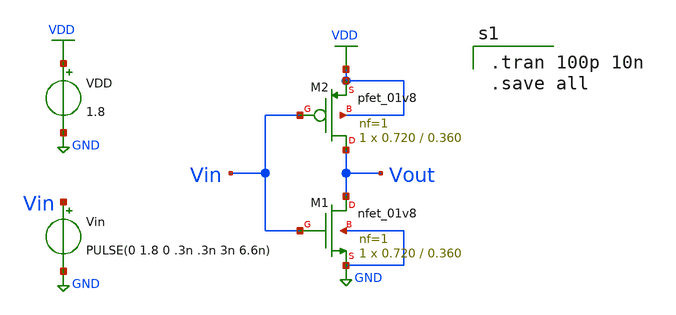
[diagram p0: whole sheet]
** sch_path: xschem/inverter/inverter_squarewave.sch
**.subckt inverter_squarewave
VDD VDD GND 1.8
Vin Vin GND PULSE(0 1.8 0 .3n .3n 3n 6.6n)
XM1 Vout Vin GND GND sky130_fd_pr__nfet_01v8 L=0.360 W=0.720 nf=1 ad='int((nf+1)/2) * W/nf * 0.29' as='int((nf+2)/2) * W/nf * 0.29'
+ pd='2*int((nf+1)/2) * (W/nf + 0.29)' ps='2*int((nf+2)/2) * (W/nf + 0.29)' nrd='0.29 / W' nrs='0.29 / W'
+ sa=0 sb=0 sd=0 mult=1 m=1
XM2 Vout Vin VDD VDD sky130_fd_pr__pfet_01v8 L=0.360 W=0.720 nf=1 ad='int((nf+1)/2) * W/nf * 0.29' as='int((nf+2)/2) * W/nf * 0.29'
+ pd='2*int((nf+1)/2) * (W/nf + 0.29)' ps='2*int((nf+2)/2) * (W/nf + 0.29)' nrd='0.29 / W' nrs='0.29 / W'
+ sa=0 sb=0 sd=0 mult=1 m=1
**** begin user architecture code

.tran 100p 10n
.save all


** opencircuitdesign pdks install
.lib $::SKYWATER_MODELS/sky130.lib.spice tt


**** end user architecture code
**.ends
.GLOBAL GND
.GLOBAL VDD
.end
